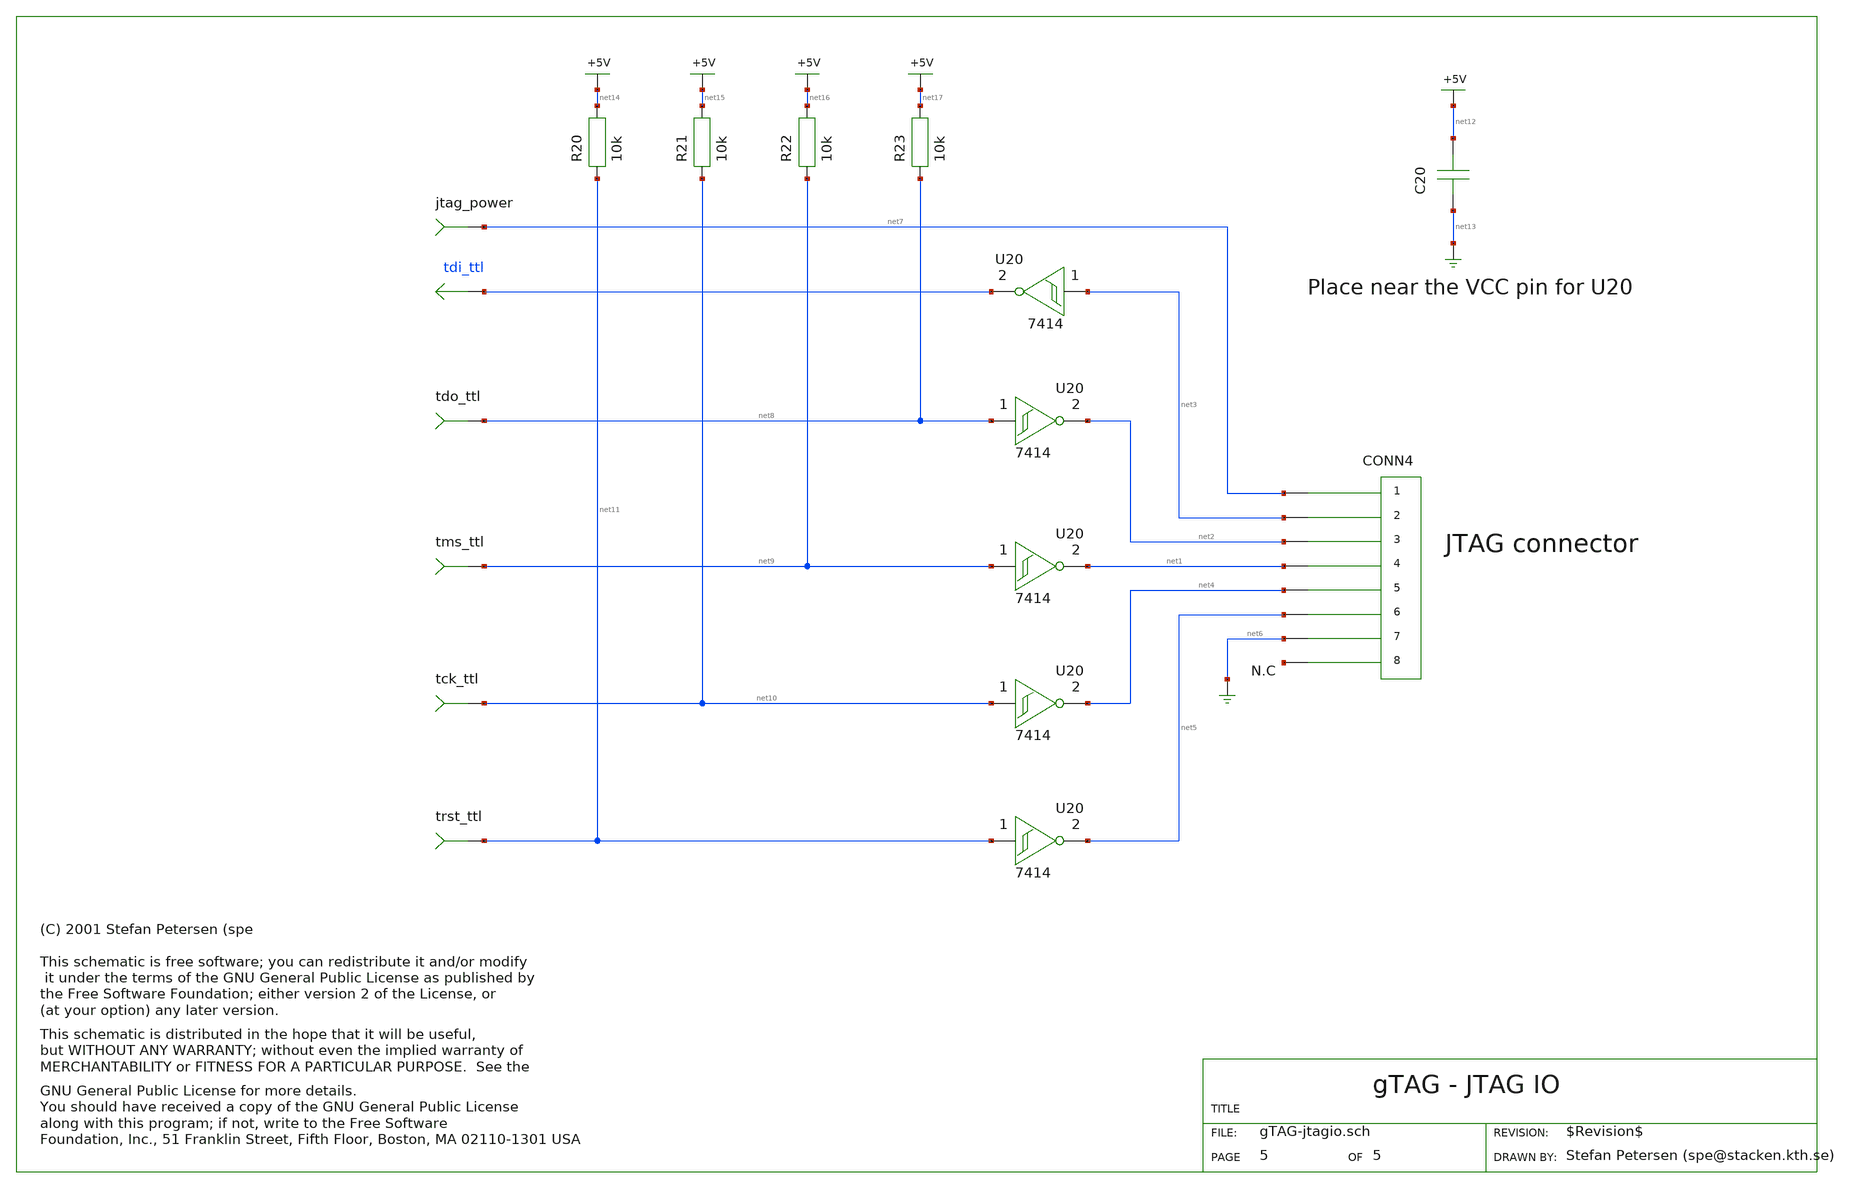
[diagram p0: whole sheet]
** sch_path: xschem_library/gschem_import/gTAG-jtagio.sch
* copyleft.sym
**.subckt gTAG-jtagio
tdo_ttl net8
tms_ttl net9
tck_ttl net10
trst_ttl net11
jtag_power net7
U20 net3 xxx
U20 net8 net2
U20 net9 net1
U20 net10 net4
U20 net11 net5
CONN4 net3 net1 net5 net18 net7 net2 net4 net6
C20 net13 net12 100n
R20 net11 net14 10k
R21 net10 net15 10k
R22 net9 net16 10k
R23 net8 net17 10k
**.ends
.end
